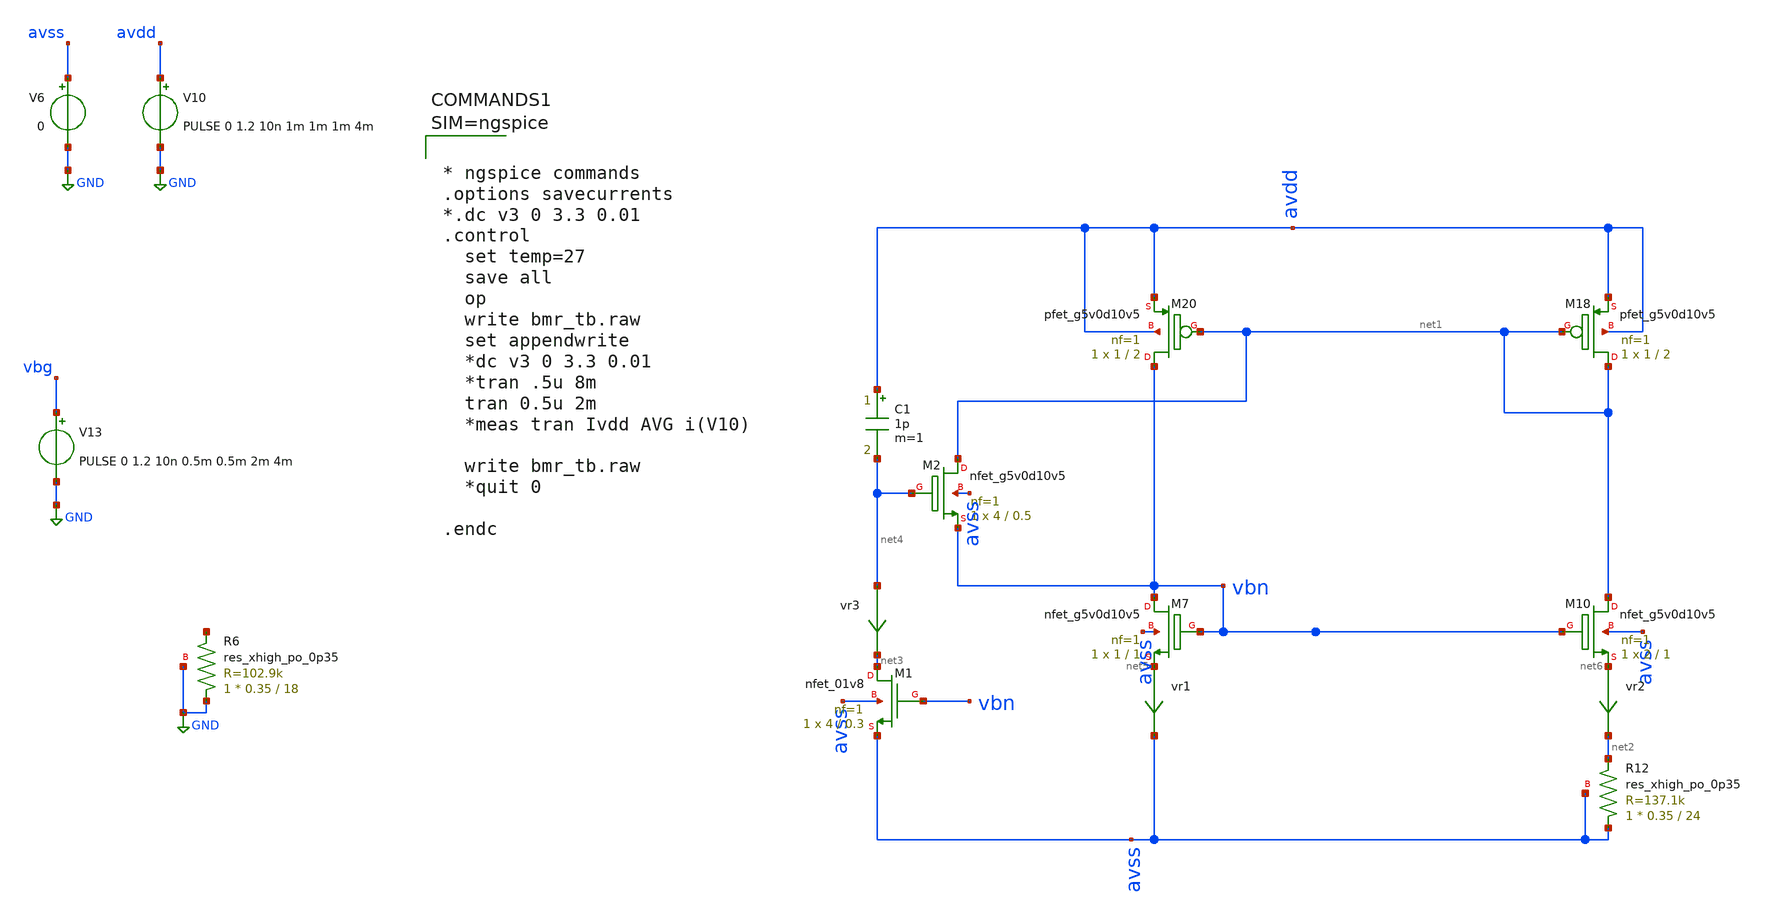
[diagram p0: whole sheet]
** sch_path: xschem/bmr_tb.sch
**.subckt bmr_tb
XM18 net1 net1 avdd avdd sky130_fd_pr__pfet_g5v0d10v5 L=2 W=1 nf=1 ad='int((nf+1)/2) * W/nf * 0.29' as='int((nf+2)/2) * W/nf * 0.29'
+ pd='2*int((nf+1)/2) * (W/nf + 0.29)' ps='2*int((nf+2)/2) * (W/nf + 0.29)' nrd='0.29 / W' nrs='0.29 / W'
+ sa=0 sb=0 sd=0 mult=1 m=1
XM20 vbn net1 avdd avdd sky130_fd_pr__pfet_g5v0d10v5 L=2 W=1 nf=1 ad='int((nf+1)/2) * W/nf * 0.29' as='int((nf+2)/2) * W/nf * 0.29'
+ pd='2*int((nf+1)/2) * (W/nf + 0.29)' ps='2*int((nf+2)/2) * (W/nf + 0.29)' nrd='0.29 / W' nrs='0.29 / W'
+ sa=0 sb=0 sd=0 mult=1 m=1
XR12 avss net2 avss sky130_fd_pr__res_xhigh_po_0p35 L=24 mult=1 m=1
vr1 net5 avss 0
.save i(vr1)
vr2 net6 net2 0
.save i(vr2)
vr3 net4 net3 0
.save i(vr3)
V10 avdd GND PULSE 0 1.2 10n 1m 1m 1m 4m
V6 avss GND 0
V13 vbg GND PULSE 0 1.2 10n 0.5m 0.5m 2m 4m
XR6 GND net7 GND sky130_fd_pr__res_xhigh_po_0p35 L=18 mult=1 m=1
XM7 vbn vbn net5 avss sky130_fd_pr__nfet_g5v0d10v5 L=1 W=1 nf=1 ad='int((nf+1)/2) * W/nf * 0.29' as='int((nf+2)/2) * W/nf * 0.29'
+ pd='2*int((nf+1)/2) * (W/nf + 0.29)' ps='2*int((nf+2)/2) * (W/nf + 0.29)' nrd='0.29 / W' nrs='0.29 / W'
+ sa=0 sb=0 sd=0 mult=1 m=1
XM10 net1 vbn net6 avss sky130_fd_pr__nfet_g5v0d10v5 L=1 W=2 nf=1 ad='int((nf+1)/2) * W/nf * 0.29' as='int((nf+2)/2) * W/nf * 0.29'
+ pd='2*int((nf+1)/2) * (W/nf + 0.29)' ps='2*int((nf+2)/2) * (W/nf + 0.29)' nrd='0.29 / W' nrs='0.29 / W'
+ sa=0 sb=0 sd=0 mult=1 m=1
C1 avdd net4 1p m=1
XM2 net1 net4 vbn avss sky130_fd_pr__nfet_g5v0d10v5 L=0.5 W=4 nf=1 ad='int((nf+1)/2) * W/nf * 0.29' as='int((nf+2)/2) * W/nf * 0.29'
+ pd='2*int((nf+1)/2) * (W/nf + 0.29)' ps='2*int((nf+2)/2) * (W/nf + 0.29)' nrd='0.29 / W' nrs='0.29 / W'
+ sa=0 sb=0 sd=0 mult=1 m=1
XM1 net3 vbn avss avss sky130_fd_pr__nfet_01v8 L=0.3 W=4 nf=1 ad='int((nf+1)/2) * W/nf * 0.29' as='int((nf+2)/2) * W/nf * 0.29'
+ pd='2*int((nf+1)/2) * (W/nf + 0.29)' ps='2*int((nf+2)/2) * (W/nf + 0.29)' nrd='0.29 / W' nrs='0.29 / W'
+ sa=0 sb=0 sd=0 mult=1 m=1
**** begin user architecture code



* ngspice commands
.options savecurrents
*.dc v3 0 3.3 0.01
.control
  set temp=27
  save all
  op
  write bmr_tb.raw
  set appendwrite
  *dc v3 0 3.3 0.01
  *tran .5u 8m
  tran 0.5u 2m
  *meas tran Ivdd AVG i(V10)

  write bmr_tb.raw
  *quit 0

.endc



 .lib $::SKYWATER_MODELS/sky130.lib.spice tt

.include $::SKYWATER_STDCELLS/sky130_fd_sc_hd.spice
.include $::SKYWATER_STDCELLS/../../sky130_fd_sc_hvl/spice/sky130_fd_sc_hvl.spice


**** end user architecture code
**.ends
.GLOBAL GND
.end
